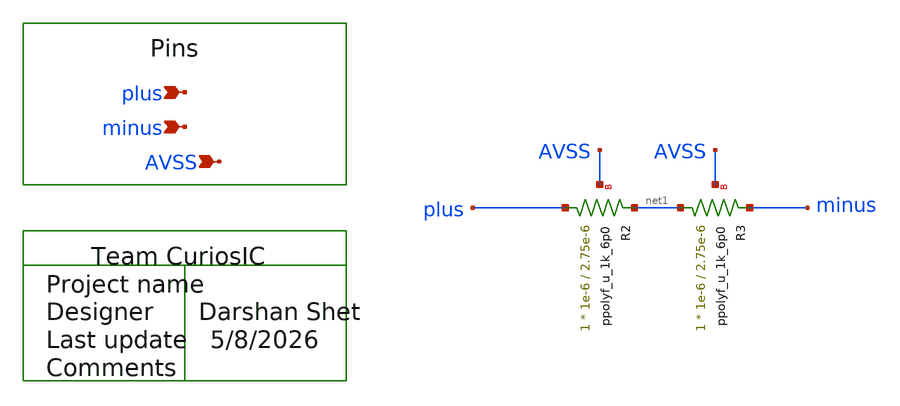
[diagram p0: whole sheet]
** sch_path: design/schematics/ADC/DSM_Loop_filter/First_int/OTA_Files/DS_cic_bms_afe_iadc_first_int_OTA_nulling_resistor.sch
**.subckt DS_cic_bms_afe_iadc_first_int_OTA_nulling_resistor plus minus AVSS
*.ipin plus
*.ipin minus
*.ipin AVSS
XR2 plus net1 AVSS ppolyf_u_1k_6p0 r_width=1e-6 r_length=2.75e-6 m=1
XR3 net1 minus AVSS ppolyf_u_1k_6p0 r_width=1e-6 r_length=2.75e-6 m=1
**.ends
.end
